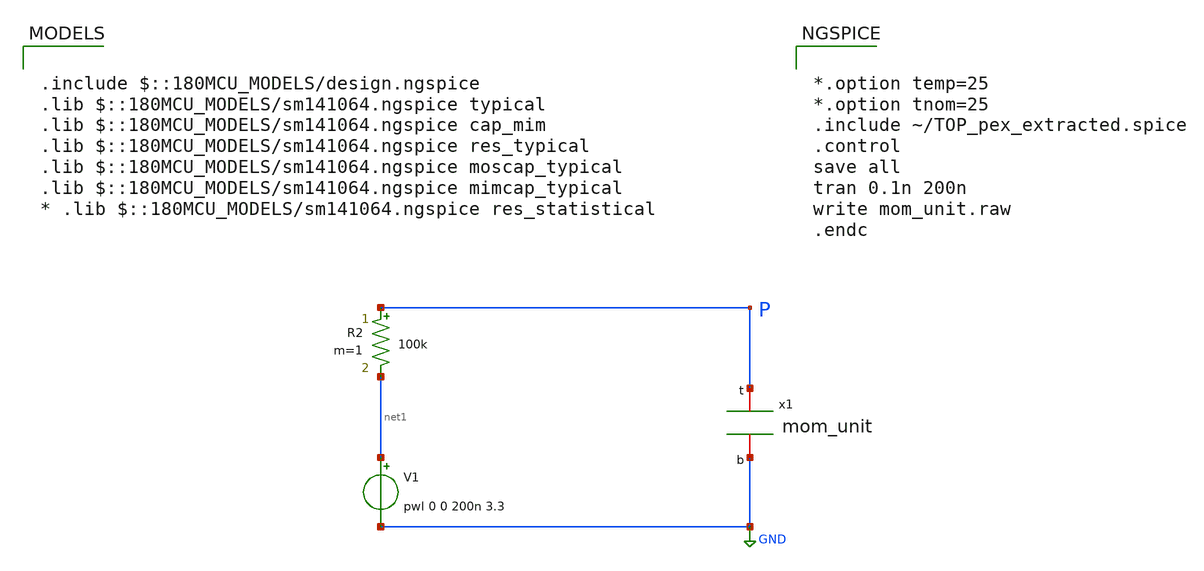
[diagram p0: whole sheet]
** sch_path: noritsuna/CDAC/mom/mom_unit.sch
**.subckt mom_unit
R2 P net1 100k m=1
V1 net1 GND pwl 0 0 200n 3.3
x1 P GND TOP
**** begin user architecture code

.include $::180MCU_MODELS/design.ngspice
.lib $::180MCU_MODELS/sm141064.ngspice typical
.lib $::180MCU_MODELS/sm141064.ngspice cap_mim
.lib $::180MCU_MODELS/sm141064.ngspice res_typical
.lib $::180MCU_MODELS/sm141064.ngspice moscap_typical
.lib $::180MCU_MODELS/sm141064.ngspice mimcap_typical
* .lib $::180MCU_MODELS/sm141064.ngspice res_statistical



*.option temp=25
*.option tnom=25
.include ~/TOP_pex_extracted.spice
.control
save all
tran 0.1n 200n
write mom_unit.raw
.endc


**** end user architecture code
**.ends
.GLOBAL GND
.end
